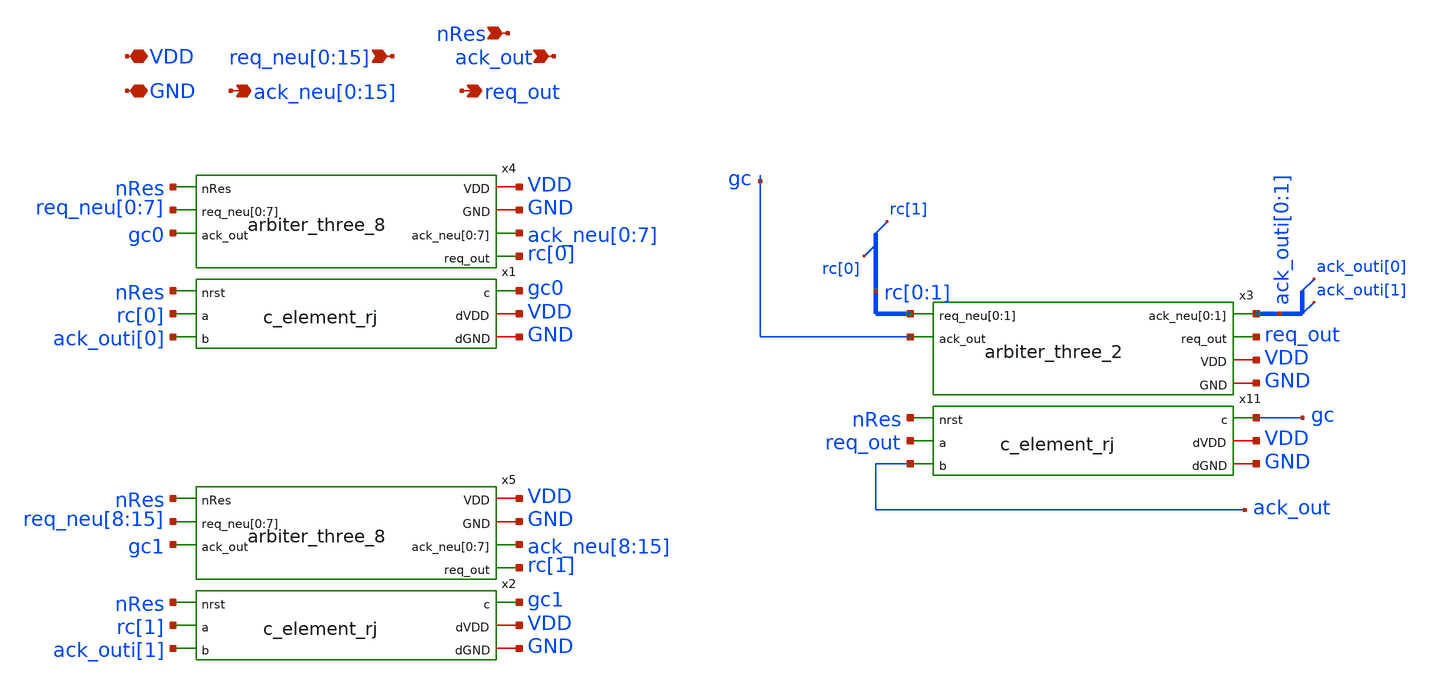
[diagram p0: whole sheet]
** sch_path: design/xschem/arbiter_three_16.sch
**.subckt arbiter_three_16 VDD GND
*+ req_neu[0],req_neu[1],req_neu[2],req_neu[3],req_neu[4],req_neu[5],req_neu[6],req_neu[7],req_neu[8],req_neu[9],req_neu[10],req_neu[11],req_neu[12],req_neu[13],req_neu[14],req_neu[15]
*+ ack_neu[0],ack_neu[1],ack_neu[2],ack_neu[3],ack_neu[4],ack_neu[5],ack_neu[6],ack_neu[7],ack_neu[8],ack_neu[9],ack_neu[10],ack_neu[11],ack_neu[12],ack_neu[13],ack_neu[14],ack_neu[15] nRes ack_out req_out
*.iopin VDD
*.iopin GND
*.ipin
*+ req_neu[0],req_neu[1],req_neu[2],req_neu[3],req_neu[4],req_neu[5],req_neu[6],req_neu[7],req_neu[8],req_neu[9],req_neu[10],req_neu[11],req_neu[12],req_neu[13],req_neu[14],req_neu[15]
*.opin
*+ ack_neu[0],ack_neu[1],ack_neu[2],ack_neu[3],ack_neu[4],ack_neu[5],ack_neu[6],ack_neu[7],ack_neu[8],ack_neu[9],ack_neu[10],ack_neu[11],ack_neu[12],ack_neu[13],ack_neu[14],ack_neu[15]
*.ipin nRes
*.ipin ack_out
*.opin req_out
x3 ack_outi[0] ack_outi[1] rc[0] rc[1] gc req_out VDD GND arbiter_three_2
x11 nRes req_out ack_out gc VDD GND c_element_rj
x4 VDD GND nRes req_neu[0] req_neu[1] req_neu[2] req_neu[3] req_neu[4] req_neu[5] req_neu[6]
+ req_neu[7] gc0 ack_neu[0] ack_neu[1] ack_neu[2] ack_neu[3] ack_neu[4] ack_neu[5] ack_neu[6] ack_neu[7] rc[0]
+ arbiter_three_8
x5 VDD GND nRes req_neu[8] req_neu[9] req_neu[10] req_neu[11] req_neu[12] req_neu[13] req_neu[14]
+ req_neu[15] gc1 ack_neu[8] ack_neu[9] ack_neu[10] ack_neu[11] ack_neu[12] ack_neu[13] ack_neu[14] ack_neu[15]
+ rc[1] arbiter_three_8
x1 nRes rc[0] ack_outi[0] gc0 VDD GND c_element_rj
x2 nRes rc[1] ack_outi[1] gc1 VDD GND c_element_rj
**.ends

* expanding   symbol:  arbiter_three_2.sym # of pins=6
** sym_path: design/xschem/arbiter_three_2.sym
** sch_path: design/xschem/arbiter_three_2.sch
.subckt arbiter_three_2 ack_neu[0] ack_neu[1] req_neu[0] req_neu[1] ack_out req_out VDD GND
*.ipin ack_out
*.opin req_out
*.ipin req_neu[0],req_neu[1]
*.opin ack_neu[0],ack_neu[1]
*.iopin VDD
*.iopin GND
x1 ack_neu[1] ack_neu[0] ack_out req_out req_neu[0] req_neu[1] VDD GND arbiter_cell_two_bits_fc
.ends


* expanding   symbol:  c_element_rj.sym # of pins=6
** sym_path: design/xschem/c_element_rj.sym
** sch_path: design/xschem/c_element_rj.sch
.subckt c_element_rj nrst a b c dVDD dGND
*.iopin dGND
*.iopin dVDD
*.opin c
*.ipin b
*.ipin a
*.ipin nrst
XM14 c net6 dVDD dVDD sky130_fd_pr__pfet_01v8 L=0.15 W=1 nf=1 ad='int((nf+1)/2) * W/nf * 0.29' as='int((nf+2)/2) * W/nf * 0.29'
+ pd='2*int((nf+1)/2) * (W/nf + 0.29)' ps='2*int((nf+2)/2) * (W/nf + 0.29)' nrd='0.29 / W' nrs='0.29 / W'
+ sa=0 sb=0 sd=0 mult=1 m=1
XM5 net6 nrst dVDD dVDD sky130_fd_pr__pfet_01v8 L=0.15 W=1 nf=1 ad='int((nf+1)/2) * W/nf * 0.29' as='int((nf+2)/2) * W/nf * 0.29'
+ pd='2*int((nf+1)/2) * (W/nf + 0.29)' ps='2*int((nf+2)/2) * (W/nf + 0.29)' nrd='0.29 / W' nrs='0.29 / W'
+ sa=0 sb=0 sd=0 mult=1 m=1
XM6 net5 b dVDD dVDD sky130_fd_pr__pfet_01v8 L=0.15 W=1 nf=1 ad='int((nf+1)/2) * W/nf * 0.29' as='int((nf+2)/2) * W/nf * 0.29'
+ pd='2*int((nf+1)/2) * (W/nf + 0.29)' ps='2*int((nf+2)/2) * (W/nf + 0.29)' nrd='0.29 / W' nrs='0.29 / W'
+ sa=0 sb=0 sd=0 mult=1 m=1
XM4 net4 a dVDD dVDD sky130_fd_pr__pfet_01v8 L=0.15 W=1 nf=1 ad='int((nf+1)/2) * W/nf * 0.29' as='int((nf+2)/2) * W/nf * 0.29'
+ pd='2*int((nf+1)/2) * (W/nf + 0.29)' ps='2*int((nf+2)/2) * (W/nf + 0.29)' nrd='0.29 / W' nrs='0.29 / W'
+ sa=0 sb=0 sd=0 mult=1 m=1
XM7 net3 b net4 dVDD sky130_fd_pr__pfet_01v8 L=0.15 W=1 nf=1 ad='int((nf+1)/2) * W/nf * 0.29' as='int((nf+2)/2) * W/nf * 0.29'
+ pd='2*int((nf+1)/2) * (W/nf + 0.29)' ps='2*int((nf+2)/2) * (W/nf + 0.29)' nrd='0.29 / W' nrs='0.29 / W'
+ sa=0 sb=0 sd=0 mult=1 m=1
XM8 net3 a net5 dVDD sky130_fd_pr__pfet_01v8 L=0.15 W=1 nf=1 ad='int((nf+1)/2) * W/nf * 0.29' as='int((nf+2)/2) * W/nf * 0.29'
+ pd='2*int((nf+1)/2) * (W/nf + 0.29)' ps='2*int((nf+2)/2) * (W/nf + 0.29)' nrd='0.29 / W' nrs='0.29 / W'
+ sa=0 sb=0 sd=0 mult=1 m=1
XM10 net5 c net4 dVDD sky130_fd_pr__pfet_01v8 L=0.15 W=1 nf=1 ad='int((nf+1)/2) * W/nf * 0.29' as='int((nf+2)/2) * W/nf * 0.29'
+ pd='2*int((nf+1)/2) * (W/nf + 0.29)' ps='2*int((nf+2)/2) * (W/nf + 0.29)' nrd='0.29 / W' nrs='0.29 / W'
+ sa=0 sb=0 sd=0 mult=1 m=1
XM12 c net6 dGND dGND sky130_fd_pr__nfet_01v8 L=0.15 W=0.65 nf=1 ad='int((nf+1)/2) * W/nf * 0.29' as='int((nf+2)/2) * W/nf * 0.29'
+ pd='2*int((nf+1)/2) * (W/nf + 0.29)' ps='2*int((nf+2)/2) * (W/nf + 0.29)' nrd='0.29 / W' nrs='0.29 / W'
+ sa=0 sb=0 sd=0 mult=1 m=1
XM1 net3 nrst net6 dGND sky130_fd_pr__nfet_01v8 L=0.15 W=0.65 nf=1 ad='int((nf+1)/2) * W/nf * 0.29' as='int((nf+2)/2) * W/nf * 0.29'
+ pd='2*int((nf+1)/2) * (W/nf + 0.29)' ps='2*int((nf+2)/2) * (W/nf + 0.29)' nrd='0.29 / W' nrs='0.29 / W'
+ sa=0 sb=0 sd=0 mult=1 m=1
XM2 net3 b net1 dGND sky130_fd_pr__nfet_01v8 L=0.15 W=0.65 nf=1 ad='int((nf+1)/2) * W/nf * 0.29' as='int((nf+2)/2) * W/nf * 0.29'
+ pd='2*int((nf+1)/2) * (W/nf + 0.29)' ps='2*int((nf+2)/2) * (W/nf + 0.29)' nrd='0.29 / W' nrs='0.29 / W'
+ sa=0 sb=0 sd=0 mult=1 m=1
XM3 net3 a net2 dGND sky130_fd_pr__nfet_01v8 L=0.15 W=0.65 nf=1 ad='int((nf+1)/2) * W/nf * 0.29' as='int((nf+2)/2) * W/nf * 0.29'
+ pd='2*int((nf+1)/2) * (W/nf + 0.29)' ps='2*int((nf+2)/2) * (W/nf + 0.29)' nrd='0.29 / W' nrs='0.29 / W'
+ sa=0 sb=0 sd=0 mult=1 m=1
XM9 net2 c net1 dGND sky130_fd_pr__nfet_01v8 L=0.15 W=0.65 nf=1 ad='int((nf+1)/2) * W/nf * 0.29' as='int((nf+2)/2) * W/nf * 0.29'
+ pd='2*int((nf+1)/2) * (W/nf + 0.29)' ps='2*int((nf+2)/2) * (W/nf + 0.29)' nrd='0.29 / W' nrs='0.29 / W'
+ sa=0 sb=0 sd=0 mult=1 m=1
XM11 net1 a dGND dGND sky130_fd_pr__nfet_01v8 L=0.15 W=0.65 nf=1 ad='int((nf+1)/2) * W/nf * 0.29' as='int((nf+2)/2) * W/nf * 0.29'
+ pd='2*int((nf+1)/2) * (W/nf + 0.29)' ps='2*int((nf+2)/2) * (W/nf + 0.29)' nrd='0.29 / W' nrs='0.29 / W'
+ sa=0 sb=0 sd=0 mult=1 m=1
XM13 net2 b dGND dGND sky130_fd_pr__nfet_01v8 L=0.15 W=0.65 nf=1 ad='int((nf+1)/2) * W/nf * 0.29' as='int((nf+2)/2) * W/nf * 0.29'
+ pd='2*int((nf+1)/2) * (W/nf + 0.29)' ps='2*int((nf+2)/2) * (W/nf + 0.29)' nrd='0.29 / W' nrs='0.29 / W'
+ sa=0 sb=0 sd=0 mult=1 m=1
.ends


* expanding   symbol:  arbiter_three_8.sym # of pins=7
** sym_path: design/xschem/arbiter_three_8.sym
** sch_path: design/xschem/arbiter_three_8.sch
.subckt arbiter_three_8 VDD GND nRes req_neu[0] req_neu[1] req_neu[2] req_neu[3] req_neu[4]
+ req_neu[5] req_neu[6] req_neu[7] ack_out ack_neu[0] ack_neu[1] ack_neu[2] ack_neu[3] ack_neu[4] ack_neu[5]
+ ack_neu[6] ack_neu[7] req_out
*.ipin ack_out
*.opin req_out
*.ipin req_neu[0],req_neu[1],req_neu[2],req_neu[3],req_neu[4],req_neu[5],req_neu[6],req_neu[7]
*.opin ack_neu[0],ack_neu[1],ack_neu[2],ack_neu[3],ack_neu[4],ack_neu[5],ack_neu[6],ack_neu[7]
*.ipin nRes
*.iopin VDD
*.iopin GND
x1 VDD GND nRes req_neu[0] req_neu[1] req_neu[2] req_neu[3] gc0 rc[0] ack_neu[0] ack_neu[1]
+ ack_neu[2] ack_neu[3] arbiter_three_4
x2 VDD GND nRes req_neu[4] req_neu[5] req_neu[6] req_neu[7] gc1 rc[1] ack_neu[4] ack_neu[5]
+ ack_neu[6] ack_neu[7] arbiter_three_4
x3 ack_outi[0] ack_outi[1] rc[0] rc[1] gc req_out VDD GND arbiter_three_2
x4 nRes rc[0] ack_outi[0] gc0 VDD GND c_element_rj
x5 nRes rc[1] ack_outi[1] gc1 VDD GND c_element_rj
x11 nRes req_out ack_out gc VDD GND c_element_rj
.ends


* expanding   symbol:  arbiter_cell_two_bits_fc.sym # of pins=8
** sym_path: design/xschem/arbiter_cell_two_bits_fc.sym
** sch_path: design/xschem/arbiter_cell_two_bits_fc.sch
.subckt arbiter_cell_two_bits_fc g1 g0 gc rc r0 r1 VDD GND
*.ipin r1
*.ipin r0
*.opin g0
*.opin g1
*.opin rc
*.ipin gc
*.iopin GND
*.iopin VDD
x1 net6 net5 GND GND VDD VDD net7 sky130_fd_sc_hd__nand2_1
x2 r0 gc GND GND VDD VDD net4 sky130_fd_sc_hd__or2_1
x3 net3 net1 GND GND VDD VDD g0 sky130_fd_sc_hd__nor2_1
x4 net6 net6 net6 net6 GND GND VDD VDD net3 sky130_fd_sc_hd__or4_1
x5 gc GND GND VDD VDD net1 sky130_fd_sc_hd__inv_1
x6 gc r1 GND GND VDD VDD net5 sky130_fd_sc_hd__or2_1
x7 net4 net7 GND GND VDD VDD net6 sky130_fd_sc_hd__nand2_1
x8 net7 net7 net7 net7 GND GND VDD VDD net2 sky130_fd_sc_hd__or4_1
x9 net1 net2 GND GND VDD VDD g1 sky130_fd_sc_hd__nor2_1
x10 net2 r0 GND GND VDD VDD net8 sky130_fd_sc_hd__nand2_1
x11 net3 r1 GND GND VDD VDD net9 sky130_fd_sc_hd__nand2_1
x12 net8 net9 GND GND VDD VDD rc sky130_fd_sc_hd__nand2_1
.ends


* expanding   symbol:  arbiter_three_4.sym # of pins=7
** sym_path: design/xschem/arbiter_three_4.sym
** sch_path: design/xschem/arbiter_three_4.sch
.subckt arbiter_three_4 VDD GND nRes req_neu[0] req_neu[1] req_neu[2] req_neu[3] ack_out req_out
+ ack_neu[0] ack_neu[1] ack_neu[2] ack_neu[3]
*.ipin ack_out
*.opin req_out
*.ipin req_neu[0],req_neu[1],req_neu[2],req_neu[3]
*.opin ack_neu[0],ack_neu[1],ack_neu[2],ack_neu[3]
*.ipin nRes
*.iopin VDD
*.iopin GND
x11 nRes req_out ack_out gc VDD GND c_element_rj
x4 nRes rc[0] ack_outi[0] gc0 VDD GND c_element_rj
x5 nRes rc[1] ack_outi[1] gc1 VDD GND c_element_rj
x1 ack_outi[0] ack_outi[1] rc[0] rc[1] gc req_out VDD GND arbiter_three_2
x2 ack_neu[0] ack_neu[1] req_neu[0] req_neu[1] gc0 rc[0] VDD GND arbiter_three_2
x3 ack_neu[2] ack_neu[3] req_neu[2] req_neu[3] gc1 rc[1] VDD GND arbiter_three_2
.ends

.end
